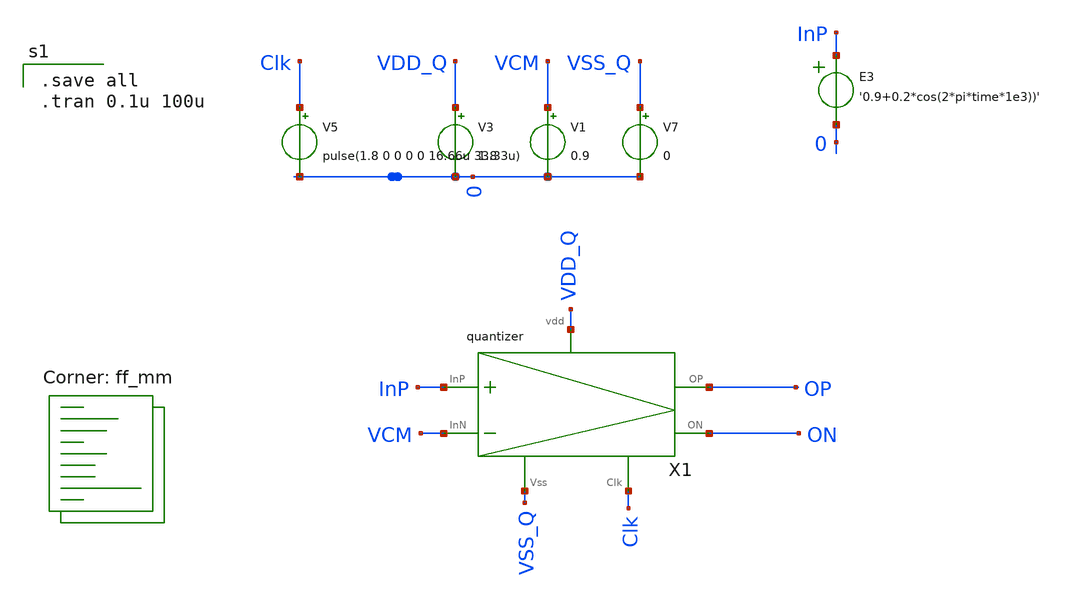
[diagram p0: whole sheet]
** sch_path: xschem/tb_quantizer.sch
**.subckt tb_quantizer
X1 VSS_Q Clk VDD_Q InP VCM OP ON quantizer
V3 VDD_Q 0 1.8
V5 Clk 0 pulse(1.8 0 0 0 0 16.66u 33.33u)
V7 VSS_Q 0 0
V1 VCM 0 0.9
E3 InP 0 VOL=' '0.9+0.2*cos(2*pi*time*1e3))' '
**** begin user architecture code
.lib $::SKYWATER_MODELS/sky130.lib.spice ff_mm

.save all
.tran 0.1u 100u


**** end user architecture code
**.ends

* expanding   symbol:  quantizer.sym # of pins=7
** sym_path: xschem/quantizer.sym
** sch_path: xschem/quantizer.sch
.subckt quantizer Vss Clk vdd InP InN OP ON
*.iopin Vss
*.iopin vdd
*.iopin Clk
*.ipin InP
*.ipin InN
*.iopin ON
*.iopin OP
XM29 nodeA1 InP net1 Vss sky130_fd_pr__nfet_01v8 L=1 W=2 nf=1 ad='int((nf+1)/2) * W/nf * 0.29' as='int((nf+2)/2) * W/nf * 0.29'
+ pd='2*int((nf+1)/2) * (W/nf + 0.29)' ps='2*int((nf+2)/2) * (W/nf + 0.29)' nrd='0.29 / W' nrs='0.29 / W'
+ sa=0 sb=0 sd=0 mult=3 m=3
XM30 NodeA2 InN net1 Vss sky130_fd_pr__nfet_01v8 L=1 W=2 nf=1 ad='int((nf+1)/2) * W/nf * 0.29' as='int((nf+2)/2) * W/nf * 0.29'
+ pd='2*int((nf+1)/2) * (W/nf + 0.29)' ps='2*int((nf+2)/2) * (W/nf + 0.29)' nrd='0.29 / W' nrs='0.29 / W'
+ sa=0 sb=0 sd=0 mult=3 m=3
XM31 OP ON NodeA2 Vss sky130_fd_pr__nfet_01v8 L=1 W=2 nf=1 ad='int((nf+1)/2) * W/nf * 0.29' as='int((nf+2)/2) * W/nf * 0.29'
+ pd='2*int((nf+1)/2) * (W/nf + 0.29)' ps='2*int((nf+2)/2) * (W/nf + 0.29)' nrd='0.29 / W' nrs='0.29 / W'
+ sa=0 sb=0 sd=0 mult=1 m=1
XM32 ON OP nodeA1 Vss sky130_fd_pr__nfet_01v8 L=1 W=2 nf=1 ad='int((nf+1)/2) * W/nf * 0.29' as='int((nf+2)/2) * W/nf * 0.29'
+ pd='2*int((nf+1)/2) * (W/nf + 0.29)' ps='2*int((nf+2)/2) * (W/nf + 0.29)' nrd='0.29 / W' nrs='0.29 / W'
+ sa=0 sb=0 sd=0 mult=1 m=1
XM34 OP ON vdd vdd sky130_fd_pr__pfet_01v8 L=1 W=4 nf=1 ad='int((nf+1)/2) * W/nf * 0.29' as='int((nf+2)/2) * W/nf * 0.29'
+ pd='2*int((nf+1)/2) * (W/nf + 0.29)' ps='2*int((nf+2)/2) * (W/nf + 0.29)' nrd='0.29 / W' nrs='0.29 / W'
+ sa=0 sb=0 sd=0 mult=1 m=1
XM35 ON OP vdd vdd sky130_fd_pr__pfet_01v8 L=1 W=4 nf=1 ad='int((nf+1)/2) * W/nf * 0.29' as='int((nf+2)/2) * W/nf * 0.29'
+ pd='2*int((nf+1)/2) * (W/nf + 0.29)' ps='2*int((nf+2)/2) * (W/nf + 0.29)' nrd='0.29 / W' nrs='0.29 / W'
+ sa=0 sb=0 sd=0 mult=1 m=1
XM36 ON Clk vdd vdd sky130_fd_pr__pfet_01v8 L=1 W=4 nf=1 ad='int((nf+1)/2) * W/nf * 0.29' as='int((nf+2)/2) * W/nf * 0.29'
+ pd='2*int((nf+1)/2) * (W/nf + 0.29)' ps='2*int((nf+2)/2) * (W/nf + 0.29)' nrd='0.29 / W' nrs='0.29 / W'
+ sa=0 sb=0 sd=0 mult=4 m=4
XM37 nodeA1 Clk vdd vdd sky130_fd_pr__pfet_01v8 L=1 W=4 nf=1 ad='int((nf+1)/2) * W/nf * 0.29' as='int((nf+2)/2) * W/nf * 0.29'
+ pd='2*int((nf+1)/2) * (W/nf + 0.29)' ps='2*int((nf+2)/2) * (W/nf + 0.29)' nrd='0.29 / W' nrs='0.29 / W'
+ sa=0 sb=0 sd=0 mult=4 m=4
XM38 OP Clk vdd vdd sky130_fd_pr__pfet_01v8 L=1 W=4 nf=1 ad='int((nf+1)/2) * W/nf * 0.29' as='int((nf+2)/2) * W/nf * 0.29'
+ pd='2*int((nf+1)/2) * (W/nf + 0.29)' ps='2*int((nf+2)/2) * (W/nf + 0.29)' nrd='0.29 / W' nrs='0.29 / W'
+ sa=0 sb=0 sd=0 mult=4 m=4
XM39 NodeA2 Clk vdd vdd sky130_fd_pr__pfet_01v8 L=1 W=4 nf=1 ad='int((nf+1)/2) * W/nf * 0.29' as='int((nf+2)/2) * W/nf * 0.29'
+ pd='2*int((nf+1)/2) * (W/nf + 0.29)' ps='2*int((nf+2)/2) * (W/nf + 0.29)' nrd='0.29 / W' nrs='0.29 / W'
+ sa=0 sb=0 sd=0 mult=4 m=4
XM1 OP Vss Vss Vss sky130_fd_pr__nfet_01v8 L=1 W=2 nf=1 ad='int((nf+1)/2) * W/nf * 0.29' as='int((nf+2)/2) * W/nf * 0.29'
+ pd='2*int((nf+1)/2) * (W/nf + 0.29)' ps='2*int((nf+2)/2) * (W/nf + 0.29)' nrd='0.29 / W' nrs='0.29 / W'
+ sa=0 sb=0 sd=0 mult=5 m=5
XM2 ON Vss Vss Vss sky130_fd_pr__nfet_01v8 L=1 W=2 nf=1 ad='int((nf+1)/2) * W/nf * 0.29' as='int((nf+2)/2) * W/nf * 0.29'
+ pd='2*int((nf+1)/2) * (W/nf + 0.29)' ps='2*int((nf+2)/2) * (W/nf + 0.29)' nrd='0.29 / W' nrs='0.29 / W'
+ sa=0 sb=0 sd=0 mult=5 m=5
XM3 ON vdd vdd vdd sky130_fd_pr__pfet_01v8 L=1 W=4 nf=1 ad='int((nf+1)/2) * W/nf * 0.29' as='int((nf+2)/2) * W/nf * 0.29'
+ pd='2*int((nf+1)/2) * (W/nf + 0.29)' ps='2*int((nf+2)/2) * (W/nf + 0.29)' nrd='0.29 / W' nrs='0.29 / W'
+ sa=0 sb=0 sd=0 mult=1 m=1
XM4 OP vdd vdd vdd sky130_fd_pr__pfet_01v8 L=1 W=4 nf=1 ad='int((nf+1)/2) * W/nf * 0.29' as='int((nf+2)/2) * W/nf * 0.29'
+ pd='2*int((nf+1)/2) * (W/nf + 0.29)' ps='2*int((nf+2)/2) * (W/nf + 0.29)' nrd='0.29 / W' nrs='0.29 / W'
+ sa=0 sb=0 sd=0 mult=1 m=1
XM5 net1 Clk Vss Vss sky130_fd_pr__nfet_01v8 L=1 W=2 nf=1 ad='int((nf+1)/2) * W/nf * 0.29' as='int((nf+2)/2) * W/nf * 0.29'
+ pd='2*int((nf+1)/2) * (W/nf + 0.29)' ps='2*int((nf+2)/2) * (W/nf + 0.29)' nrd='0.29 / W' nrs='0.29 / W'
+ sa=0 sb=0 sd=0 mult=4 m=4
XM6 nodeA1 vdd vdd vdd sky130_fd_pr__pfet_01v8 L=1 W=4 nf=1 ad='int((nf+1)/2) * W/nf * 0.29' as='int((nf+2)/2) * W/nf * 0.29'
+ pd='2*int((nf+1)/2) * (W/nf + 0.29)' ps='2*int((nf+2)/2) * (W/nf + 0.29)' nrd='0.29 / W' nrs='0.29 / W'
+ sa=0 sb=0 sd=0 mult=1 m=1
XM7 NodeA2 vdd vdd vdd sky130_fd_pr__pfet_01v8 L=1 W=4 nf=1 ad='int((nf+1)/2) * W/nf * 0.29' as='int((nf+2)/2) * W/nf * 0.29'
+ pd='2*int((nf+1)/2) * (W/nf + 0.29)' ps='2*int((nf+2)/2) * (W/nf + 0.29)' nrd='0.29 / W' nrs='0.29 / W'
+ sa=0 sb=0 sd=0 mult=1 m=1
.ends

.end
